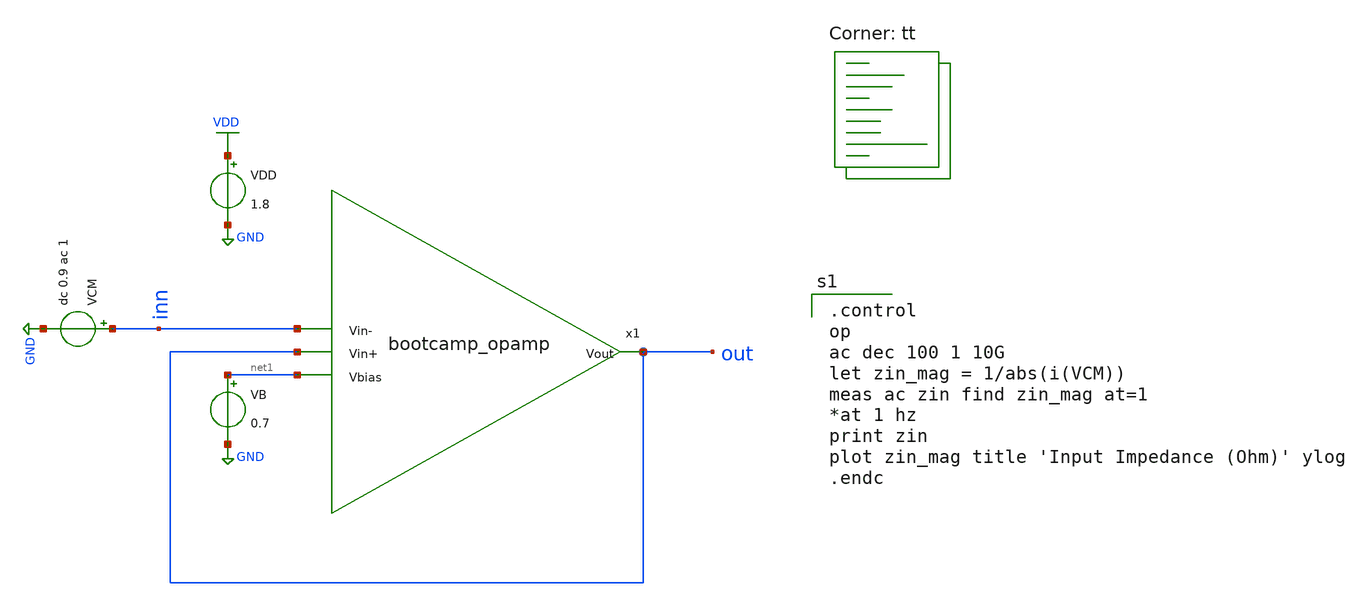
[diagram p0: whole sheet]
** sch_path: analog/schematics/tb_input_impedance.sch
**.subckt tb_input_impedance
x1 out inn out net1 bootcamp_opamp
VDD VDD GND 1.8
VB net1 GND 0.7
VCM inn GND dc 0.9 ac 1
**** begin user architecture code

.control
op
ac dec 100 1 10G
let zin_mag = 1/abs(i(VCM))
meas ac zin find zin_mag at=1
*at 1 hz
print zin
plot zin_mag title 'Input Impedance (Ohm)' ylog
.endc

.lib $::SKYWATER_MODELS/sky130.lib.spice tt
**** end user architecture code
**.ends
.GLOBAL GND
.GLOBAL VDD
.end
